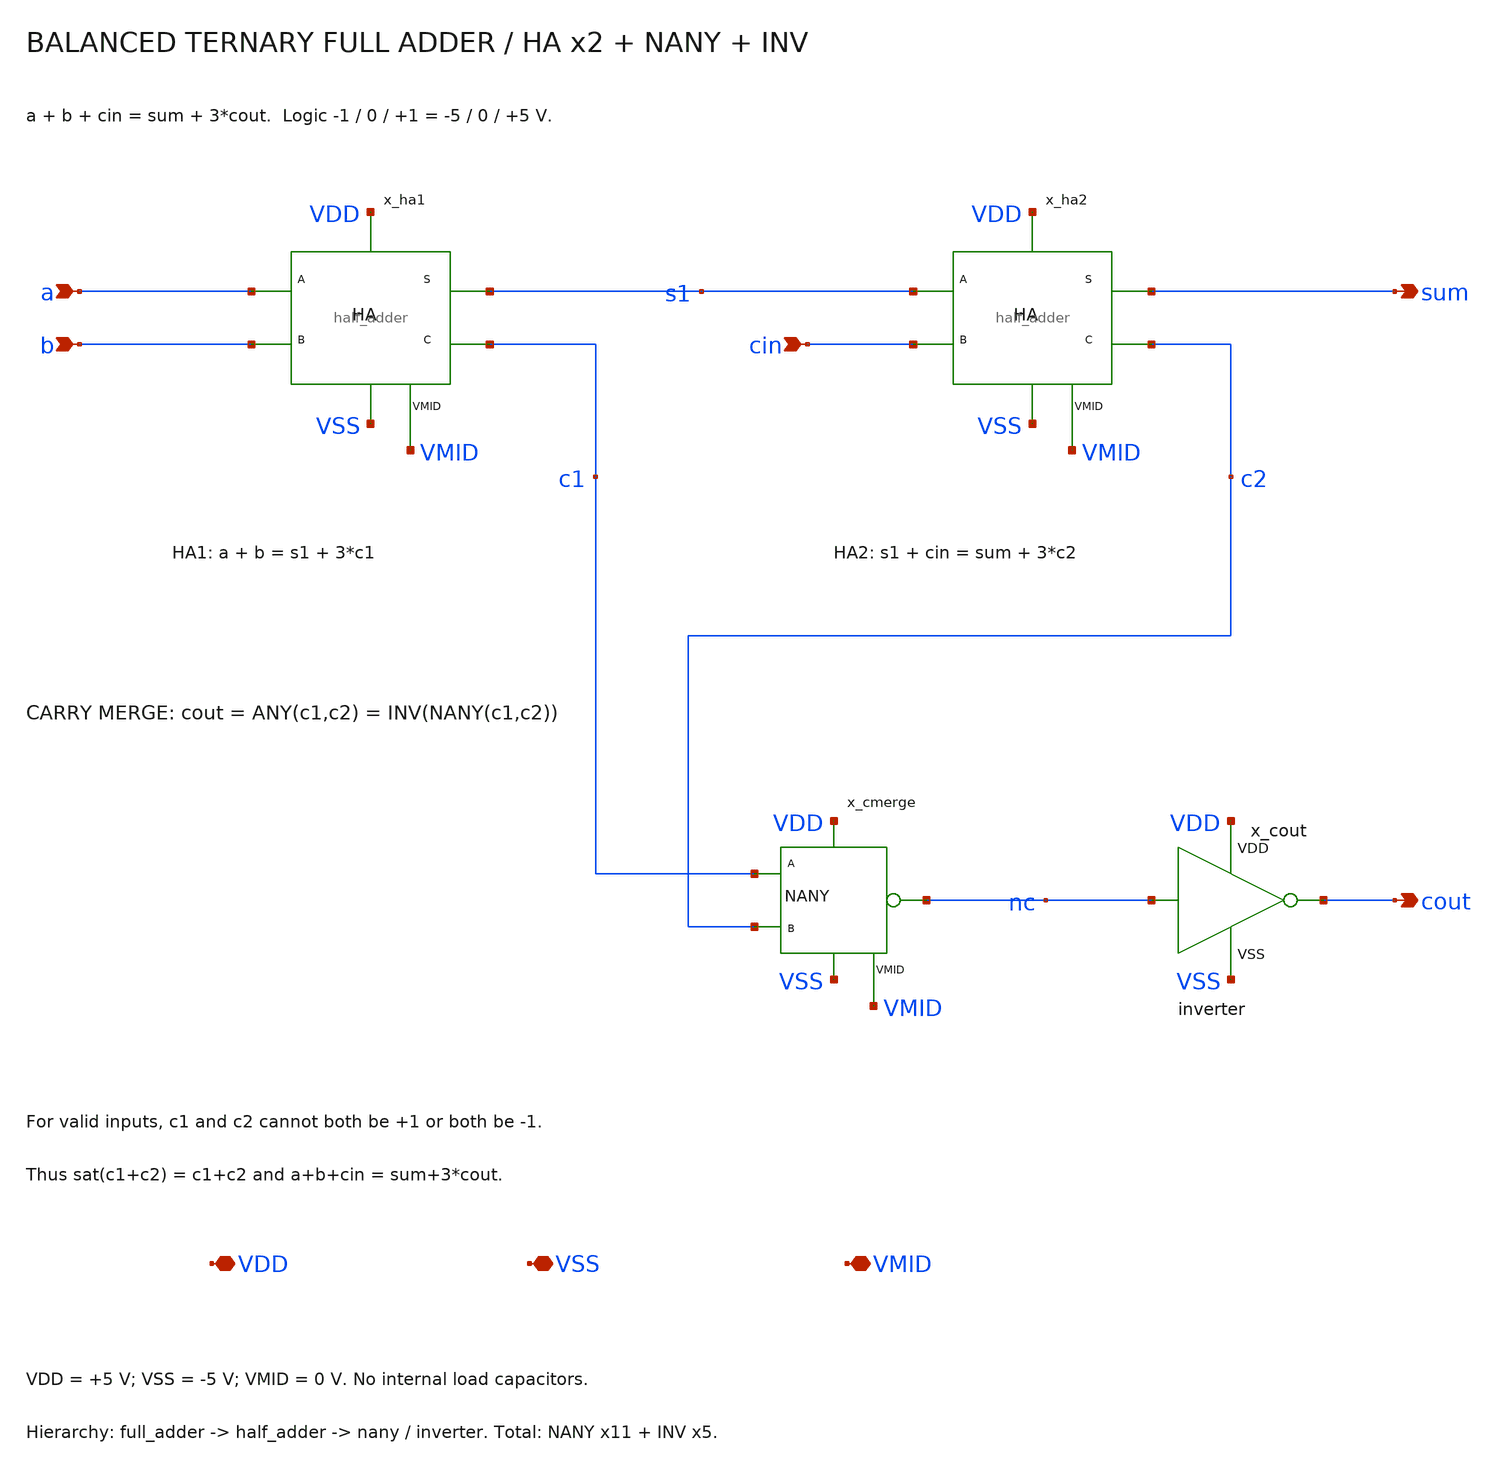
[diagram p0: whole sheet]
** sch_path: member_project/balanced-ternary-logic/PenguinEino/full_adder.sch
**.subckt full_adder a b cin sum cout VDD VSS VMID
*.ipin a
*.ipin b
*.ipin cin
*.opin sum
*.opin cout
*.iopin VDD
*.iopin VSS
*.iopin VMID
x_ha1 a b s1 c1 VDD VSS VMID half_adder
x_ha2 s1 cin sum c2 VDD VSS VMID half_adder
x_cmerge c1 c2 nc VDD VSS VMID nany
x_cout nc cout VDD VSS inverter
**.ends

* expanding   symbol:  /home/ishi-kai/balanced-ternary-logic/half_adder.sym # of pins=7
** sym_path: member_project/balanced-ternary-logic/PenguinEino/half_adder.sym
** sch_path: member_project/balanced-ternary-logic/PenguinEino/half_adder.sch
.subckt half_adder a b sum carry VDD VSS VMID
*.ipin a
*.ipin b
*.opin carry
*.iopin VDD
*.iopin VSS
*.iopin VMID
*.opin sum
x_t a b t VDD VSS VMID nany
x_u b t u VDD VSS VMID nany
x_na a na VDD VSS inverter
x_c na u carry VDD VSS VMID nany
x_d t carry d VDD VSS VMID nany
x_nd d nd VDD VSS inverter
x_s nd carry sum VDD VSS VMID nany
.ends


* expanding   symbol:  /home/ishi-kai/balanced-ternary-logic/nany.sym # of pins=6
** sym_path: member_project/balanced-ternary-logic/PenguinEino/submission/nany.sym
** sch_path: member_project/balanced-ternary-logic/PenguinEino/submission/nany.sch
.subckt nany a b vout VDD VSS VMID
*.iopin VDD
*.ipin a
*.ipin b
*.opin vout
*.iopin VSS
*.iopin VMID
XXM3 net2 b net1 VDD PMOS w=34u l=1u nrd=0 nrs=0 m=1
XR2 net2 vout VDD F_RR w=2.8e-06 l=30e-06 R=1 tc1=0 tc2=0 m=1
XR1 vout net3 VDD F_RR w=2.8e-06 l=30e-06 R=1 tc1=0 tc2=0 m=1
XXM2 net3 a net4 VSS NMOS w=11u l=1u nrd=0 nrs=0 m=1
XXM1 net4 b VSS VSS NMOS w=11u l=1u nrd=0 nrs=0 m=1
XXM5 net1 a VDD VDD PMOS w=34u l=1u nrd=0 nrs=0 m=1
XXM6 net5 a vout VDD PMOS w=14u l=1u nrd=0 nrs=0 m=1
XXM7 net5 b VMID VSS NMOS w=8u l=1u nrd=0 nrs=0 m=1
XXM8 net6 b vout VDD PMOS w=14u l=1u nrd=0 nrs=0 m=1
XXM9 net6 a VMID VSS NMOS w=8u l=1u nrd=0 nrs=0 m=1
.ends


* expanding   symbol:  /home/ishi-kai/balanced-ternary-logic/inverter.sym # of pins=4
** sym_path: member_project/balanced-ternary-logic/PenguinEino/inverter.sym
** sch_path: member_project/balanced-ternary-logic/PenguinEino/inverter.sch
.subckt inverter vin vout VDD VSS
*.iopin VDD
*.ipin vin
*.opin vout
*.iopin VSS
XXM1 net1 vin VDD VDD PMOS w=13.5u l=1u nrd=0 nrs=0 m=1
XR1 net1 vout VDD F_RR w=2.8e-06 l=30e-06 R=1 tc1=0 tc2=0 m=1
XR2 vout net2 VDD F_RR w=2.8e-06 l=30e-06 R=1 tc1=0 tc2=0 m=1
XXM2 net2 vin VSS VSS NMOS w=5u l=1u nrd=0 nrs=0 m=1
.ends

.end
